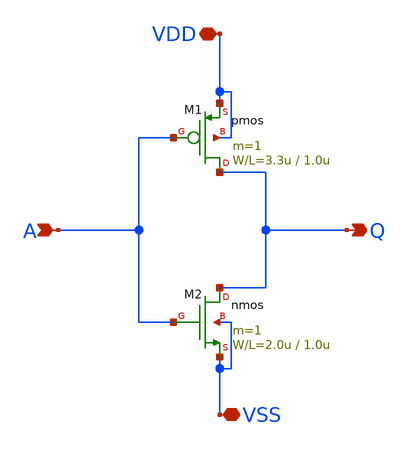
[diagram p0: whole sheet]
** sch_path: samples/inverter/PTC06/inverter.sch
**.subckt inverter A Q VDD VSS
*.ipin A
*.opin Q
*.iopin VDD
*.iopin VSS
M1 Q A VDD VDD pmos L=1.0u W=3.3u m=1
M2 Q A VSS VSS nmos L=1.0u W=2.0u m=1
**.ends
.end
